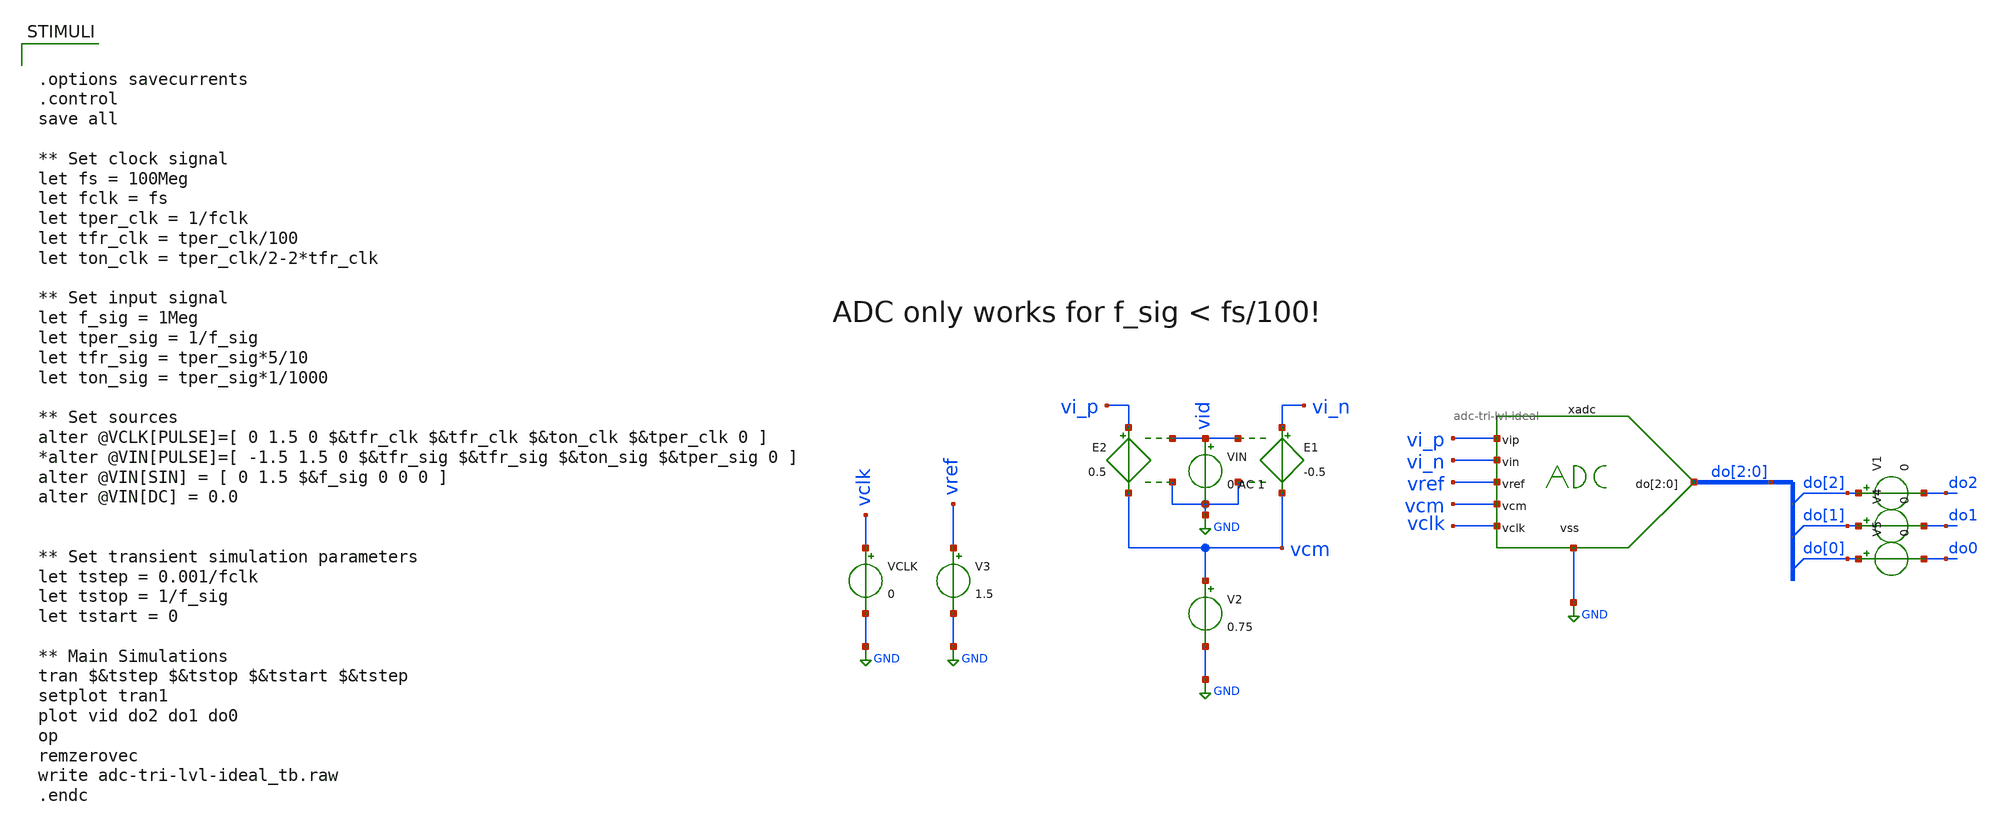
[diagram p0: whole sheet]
** sch_path: xschem/adc-tri-lvl-ideal_tb.sch
**.subckt adc-tri-lvl-ideal_tb
V2 vcm GND 0.75
E1 vi_n vcm vid GND -0.5
E2 vi_p vcm vid GND 0.5
VIN vid GND 0 AC 1
VCLK vclk GND 0
V3 vref GND 1.5
xadc do[2] do[1] do[0] vi_p vi_n vref vcm vclk GND adc-tri-lvl-ideal
V1 do[2] do2 0
V4 do[1] do1 0
V5 do[0] do0 0
**** begin user architecture code


.options savecurrents
.control
save all

** Set clock signal
let fs = 100Meg
let fclk = fs
let tper_clk = 1/fclk
let tfr_clk = tper_clk/100
let ton_clk = tper_clk/2-2*tfr_clk

** Set input signal
let f_sig = 1Meg
let tper_sig = 1/f_sig
let tfr_sig = tper_sig*5/10
let ton_sig = tper_sig*1/1000

** Set sources
alter @VCLK[PULSE]=[ 0 1.5 0 $&tfr_clk $&tfr_clk $&ton_clk $&tper_clk 0 ]
*alter @VIN[PULSE]=[ -1.5 1.5 0 $&tfr_sig $&tfr_sig $&ton_sig $&tper_sig 0 ]
alter @VIN[SIN] = [ 0 1.5 $&f_sig 0 0 0 ]
alter @VIN[DC] = 0.0


** Set transient simulation parameters
let tstep = 0.001/fclk
let tstop = 1/f_sig
let tstart = 0

** Main Simulations
tran $&tstep $&tstop $&tstart $&tstep
setplot tran1
plot vid do2 do1 do0
op
remzerovec
write adc-tri-lvl-ideal_tb.raw
.endc

**** end user architecture code
**.ends

* expanding   symbol:  adc-tri-lvl-ideal.sym # of pins=7
** sym_path: xschem/adc-tri-lvl-ideal.sym
** sch_path: xschem/adc-tri-lvl-ideal.sch
.subckt adc-tri-lvl-ideal do[2] do[1] do[0] vip vin vref vcm vclk vss
*.iopin vss
*.ipin vip
*.ipin vin
*.ipin vref
*.ipin vcm
*.ipin vclk
*.opin do[2],do[1],do[0]
xcomp1 D1 vip vin vcm vref vss comp-macro
xcomp2 D0 vip vin vref vcm vss comp-macro
**** begin user architecture code


a21 D0 CLK NULL NULL %d(Q0 NQ0) dff1
a22 D1 CLK NULL NULL %d(Q1 NQ1) dff1


**** end user architecture code
**** begin user architecture code


.model adc_buf adc_bridge(in_low=0.7499 in_high=0.7501)
.model dac1 dac_bridge(out_low = 0 out_high = 1.5 out_undef = 0 input_load = 0.1e-15 t_rise =
+ 0.01e-9 t_fall = 0.01e-9)
.model inv1 d_inverter(rise_delay = 0.01e-9 fall_delay = 0.01e-9 input_load = 0.1e-15)
.model and1 d_and(rise_delay = 0.01e-9 fall_delay = 0.01e-9 input_load = 0.01e-15)
.model dff1 d_dff(clk_delay = 0.01e-9 set_delay = 0.01e-9 reset_delay = 0.01e-9 ic = 0 rise_delay =
+ 0.01e-9 fall_delay = 0.01e-9)

**** end user architecture code
A1 [ vclk ] [ CLK ] adc_buf
A3 [ H1 ] [ do1 ] dac1
A4 [ H2 ] [ do2 ] dac1
**** begin user architecture code


a23 [NQ1 Q0] %d(H0) and1
a24 [NQ1 NQ0] %d(H1) and1
a25 [Q1 Q0] %d(H2) and1


**** end user architecture code
A2 [ H0 ] [ do0 ] dac1
V1 do2 do[2] 0
V2 do1 do[1] 0
V3 do0 do[0] 0
.ends


* expanding   symbol:  comp-macro.sym # of pins=6
** sym_path: xschem/comp-macro.sym
** sch_path: xschem/comp-macro.sch
.subckt comp-macro do vip_1 vin_1 vip_2 vin_2 vss
*.iopin vss
*.ipin vip_1
*.ipin vin_1
*.ipin vip_2
*.ipin vin_2
*.opin do
A1 [ net1 ] [ do ] comp0
E1 net1 net2 vip_1 vin_1 1
E2 net2 vss vip_2 vin_2 1
**** begin user architecture code

.model comp0 adc_bridge(in_low=-0.0001 in_high=0.0001)

**** end user architecture code
.ends

.GLOBAL GND
.end
